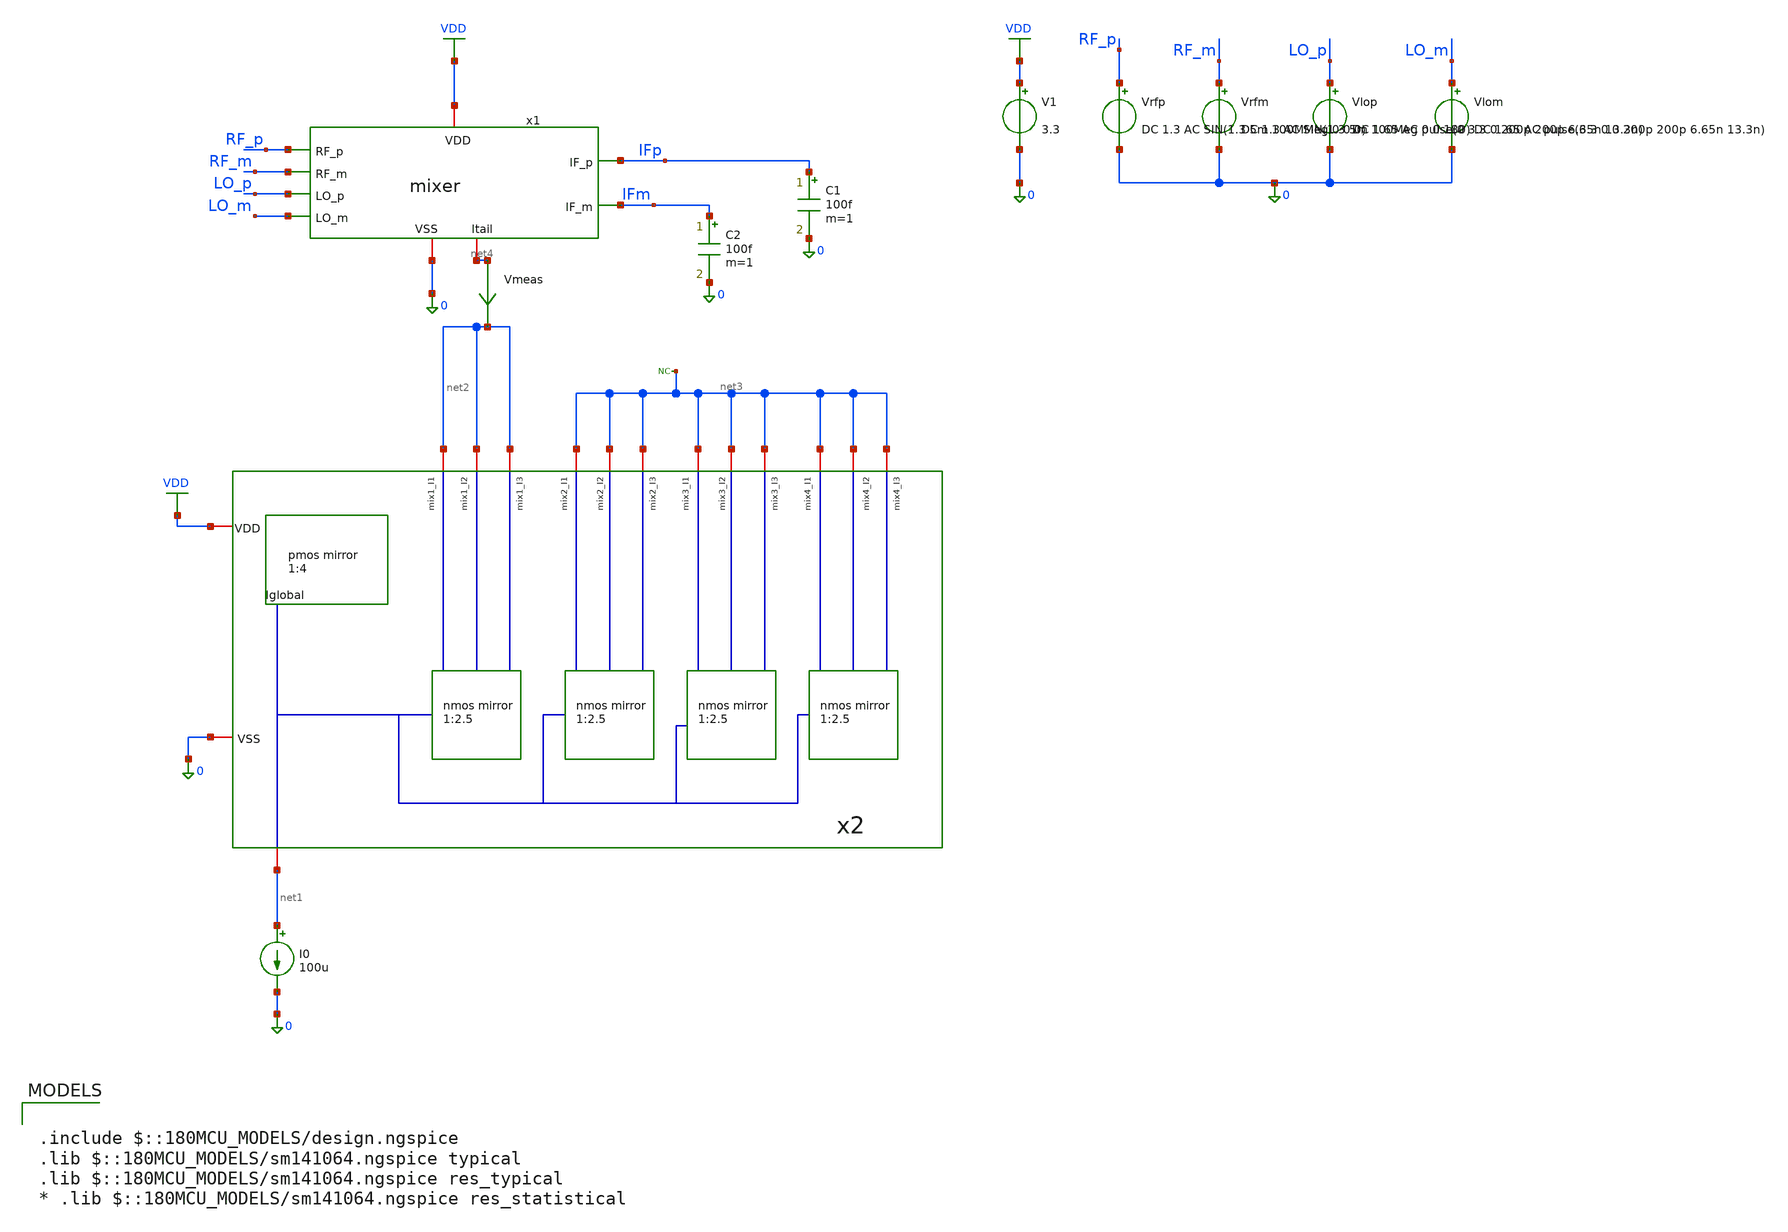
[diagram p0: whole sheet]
** sch_path: designs/mixer/testbench/mixer_with_mirror_tb.sch
**.subckt mixer_with_mirror_tb
V1 VDD 0 3.3
Vrfp RF_p 0 DC 1.3 AC SIN(1.3 5m 100MMeg 0 0 0)
Vrfm RF_m 0 DC 1.3 AC SIN(1.3 5m 100Meg 0 0 180)
Vlop LO_p 0 DC 1.65 AC pulse(0 3.3 0 200p 200p 6.65n 13.3n)
Vlom LO_m 0 DC 1.65 AC pulse(3.3 0 0 200p 200p 6.65n 13.3n)
C1 IFp 0 100f m=1
C2 IFm 0 100f m=1
x2 VDD net1 net3 net2 net3 net3 net2 net2 0 net3 net3 net3 net3 net3 net3 mirror_network
I0 net1 0 100u
* noconn #net3
x1 IFp RF_p VDD 0 IFm RF_m LO_p net4 LO_m mixer
Vmeas net4 net2 0
.save i(vmeas)
**** begin user architecture code

.include $::180MCU_MODELS/design.ngspice
.lib $::180MCU_MODELS/sm141064.ngspice typical
.lib $::180MCU_MODELS/sm141064.ngspice res_typical
* .lib $::180MCU_MODELS/sm141064.ngspice res_statistical




.control

destroy all
save all
write mixer_tb.raw

op
echo RF pair
print @m.x1.xm1.m0[gm]
print @m.x1.xm1.m0[id]
print @m.x1.xm1.m0[vgs]
print @m.x1.xm1.m0[vds]
print @m.x1.xm1.m0[vdsat]

echo LO pair
print @m.x1.xm3.m0[gm]
print @m.x1.xm3.m0[id]
print @m.x1.xm3.m0[vgs]
print @m.x1.xm3.m0[vds]
print @m.x1.xm3.m0[vdsat]

echo nmos tail
print @m.x2.x2.xm2.m0[gm]
print @m.x2.x2.xm2.m0[id]
print @m.x2.x2.xm2.m0[vgs]
print @m.x2.x2.xm2.m0[vds]
print @m.x2.x2.xm2.m0[vdsat]

print i(vmeas)
tran 0.01n 2u ;transient sim
let vrf = V(RF_p)-V(RF_m)
let vif = V(IFp)-V(IFm)

plot V(LO_p)
plot vrf
plot vif

fft vif vrf

plot mag(vif) vs frequency
.endc


**** end user architecture code
**.ends

* expanding   symbol:  /foss/designs/NYCMOS/designs/mirrors/schematic/mirror_network.sym # of
*+ pins=15
** sym_path: designs/mirrors/schematic/mirror_network.sym
** sch_path: designs/mirrors/schematic/mirror_network.sch
.subckt mirror_network VDD Iglobal mix4_I1 mix1_I1 mix4_I2 mix4_I3 mix1_I2 mix1_I3 VSS mix3_I1
+ mix3_I2 mix3_I3 mix2_I1 mix2_I2 mix2_I3
*.iopin VSS
*.iopin VDD
*.iopin Iglobal
*.iopin mix1_I1
*.iopin mix1_I2
*.iopin mix1_I3
*.iopin mix2_I1
*.iopin mix2_I2
*.iopin mix2_I3
*.iopin mix3_I1
*.iopin mix3_I2
*.iopin mix3_I3
*.iopin mix4_I1
*.iopin mix4_I2
*.iopin mix4_I3
x1 VDD net1 Iglobal pmos_mirror
x2 net1 mix1_I1 mix1_I2 mix1_I3 VSS nmos_mirror
x3 net1 mix2_I1 mix2_I2 mix2_I3 VSS nmos_mirror
x4 net1 mix3_I1 mix3_I2 mix3_I3 VSS nmos_mirror
x5 net1 mix4_I1 mix4_I2 mix4_I3 VSS nmos_mirror
.ends


* expanding   symbol:  /foss/designs/NYCMOS/designs/mixer/schematic/mixer.sym # of pins=9
** sym_path: designs/mixer/schematic/mixer.sym
** sch_path: designs/mixer/schematic/mixer.sch
.subckt mixer IF_p RF_p VDD VSS IF_m RF_m LO_p Itail LO_m
*.iopin VDD
*.ipin LO_p
*.ipin LO_m
*.iopin Itail
*.opin IF_m
*.opin IF_p
*.iopin VSS
*.ipin RF_p
*.ipin RF_m
XM1 net1 RF_p Itail VSS nfet_03v3 L=0.28u W=36u nf=6 ad='int((nf+1)/2) * W/nf * 0.18u' as='int((nf+2)/2) * W/nf * 0.18u'
+ pd='2*int((nf+1)/2) * (W/nf + 0.18u)' ps='2*int((nf+2)/2) * (W/nf + 0.18u)' nrd='0.18u / W' nrs='0.18u / W'
+ sa=0 sb=0 sd=0 m=1
XM2 net2 RF_m Itail VSS nfet_03v3 L=0.28u W=36u nf=6 ad='int((nf+1)/2) * W/nf * 0.18u' as='int((nf+2)/2) * W/nf * 0.18u'
+ pd='2*int((nf+1)/2) * (W/nf + 0.18u)' ps='2*int((nf+2)/2) * (W/nf + 0.18u)' nrd='0.18u / W' nrs='0.18u / W'
+ sa=0 sb=0 sd=0 m=1
XM3 IF_m LO_p net1 VSS nfet_03v3 L=0.28u W=21u nf=7 ad='int((nf+1)/2) * W/nf * 0.18u' as='int((nf+2)/2) * W/nf * 0.18u'
+ pd='2*int((nf+1)/2) * (W/nf + 0.18u)' ps='2*int((nf+2)/2) * (W/nf + 0.18u)' nrd='0.18u / W' nrs='0.18u / W'
+ sa=0 sb=0 sd=0 m=1
XM4 IF_p LO_m net1 VSS nfet_03v3 L=0.28u W=21u nf=7 ad='int((nf+1)/2) * W/nf * 0.18u' as='int((nf+2)/2) * W/nf * 0.18u'
+ pd='2*int((nf+1)/2) * (W/nf + 0.18u)' ps='2*int((nf+2)/2) * (W/nf + 0.18u)' nrd='0.18u / W' nrs='0.18u / W'
+ sa=0 sb=0 sd=0 m=1
XM5 IF_m LO_m net2 VSS nfet_03v3 L=0.28u W=21u nf=7 ad='int((nf+1)/2) * W/nf * 0.18u' as='int((nf+2)/2) * W/nf * 0.18u'
+ pd='2*int((nf+1)/2) * (W/nf + 0.18u)' ps='2*int((nf+2)/2) * (W/nf + 0.18u)' nrd='0.18u / W' nrs='0.18u / W'
+ sa=0 sb=0 sd=0 m=1
XM6 IF_p LO_p net2 VSS nfet_03v3 L=0.28u W=21u nf=7 ad='int((nf+1)/2) * W/nf * 0.18u' as='int((nf+2)/2) * W/nf * 0.18u'
+ pd='2*int((nf+1)/2) * (W/nf + 0.18u)' ps='2*int((nf+2)/2) * (W/nf + 0.18u)' nrd='0.18u / W' nrs='0.18u / W'
+ sa=0 sb=0 sd=0 m=1
XR1 IF_m VDD VSS ppolyf_u_1k r_width=1e-6 r_length=1.8e-6 m=1
XR2 IF_p VDD VSS ppolyf_u_1k r_width=1e-6 r_length=1.8e-6 m=1
.ends


* expanding   symbol:  /foss/designs/NYCMOS/designs/mirrors/schematic/pmos_mirror.sym # of pins=3
** sym_path: designs/mirrors/schematic/pmos_mirror.sym
** sch_path: designs/mirrors/schematic/pmos_mirror.sch
.subckt pmos_mirror VDD Iout Iref
*.iopin Iref
*.iopin Iout
*.iopin VDD
XM1 Iref Iref VDD VDD pfet_03v3 L=0.5u W=28u nf=7 ad='int((nf+1)/2) * W/nf * 0.18u' as='int((nf+2)/2) * W/nf * 0.18u'
+ pd='2*int((nf+1)/2) * (W/nf + 0.18u)' ps='2*int((nf+2)/2) * (W/nf + 0.18u)' nrd='0.18u / W' nrs='0.18u / W'
+ sa=0 sb=0 sd=0 m=1
XM2 Iout Iref VDD VDD pfet_03v3 L=0.5u W=28u nf=7 ad='int((nf+1)/2) * W/nf * 0.18u' as='int((nf+2)/2) * W/nf * 0.18u'
+ pd='2*int((nf+1)/2) * (W/nf + 0.18u)' ps='2*int((nf+2)/2) * (W/nf + 0.18u)' nrd='0.18u / W' nrs='0.18u / W'
+ sa=0 sb=0 sd=0 m=1
.ends


* expanding   symbol:  /foss/designs/NYCMOS/designs/mirrors/schematic/nmos_mirror.sym # of pins=5
** sym_path: designs/mirrors/schematic/nmos_mirror.sym
** sch_path: designs/mirrors/schematic/nmos_mirror.sch
.subckt nmos_mirror Ilocal I1_250u I2_250u I3_250u VSS
*.iopin VSS
*.iopin Ilocal
*.iopin I1_250u
*.iopin I2_250u
*.iopin I3_250u
XM1 Ilocal Ilocal VSS VSS nfet_03v3 L=0.5u W=8u nf=2 ad='int((nf+1)/2) * W/nf * 0.18u' as='int((nf+2)/2) * W/nf * 0.18u'
+ pd='2*int((nf+1)/2) * (W/nf + 0.18u)' ps='2*int((nf+2)/2) * (W/nf + 0.18u)' nrd='0.18u / W' nrs='0.18u / W'
+ sa=0 sb=0 sd=0 m=1
XM2 I1_250u Ilocal VSS VSS nfet_03v3 L=0.5u W=20u nf=5 ad='int((nf+1)/2) * W/nf * 0.18u' as='int((nf+2)/2) * W/nf * 0.18u'
+ pd='2*int((nf+1)/2) * (W/nf + 0.18u)' ps='2*int((nf+2)/2) * (W/nf + 0.18u)' nrd='0.18u / W' nrs='0.18u / W'
+ sa=0 sb=0 sd=0 m=1
XM3 I2_250u Ilocal VSS VSS nfet_03v3 L=0.5u W=20u nf=5 ad='int((nf+1)/2) * W/nf * 0.18u' as='int((nf+2)/2) * W/nf * 0.18u'
+ pd='2*int((nf+1)/2) * (W/nf + 0.18u)' ps='2*int((nf+2)/2) * (W/nf + 0.18u)' nrd='0.18u / W' nrs='0.18u / W'
+ sa=0 sb=0 sd=0 m=1
XM4 I3_250u Ilocal VSS VSS nfet_03v3 L=0.5u W=20u nf=5 ad='int((nf+1)/2) * W/nf * 0.18u' as='int((nf+2)/2) * W/nf * 0.18u'
+ pd='2*int((nf+1)/2) * (W/nf + 0.18u)' ps='2*int((nf+2)/2) * (W/nf + 0.18u)' nrd='0.18u / W' nrs='0.18u / W'
+ sa=0 sb=0 sd=0 m=1
.ends

.GLOBAL VDD
.end
